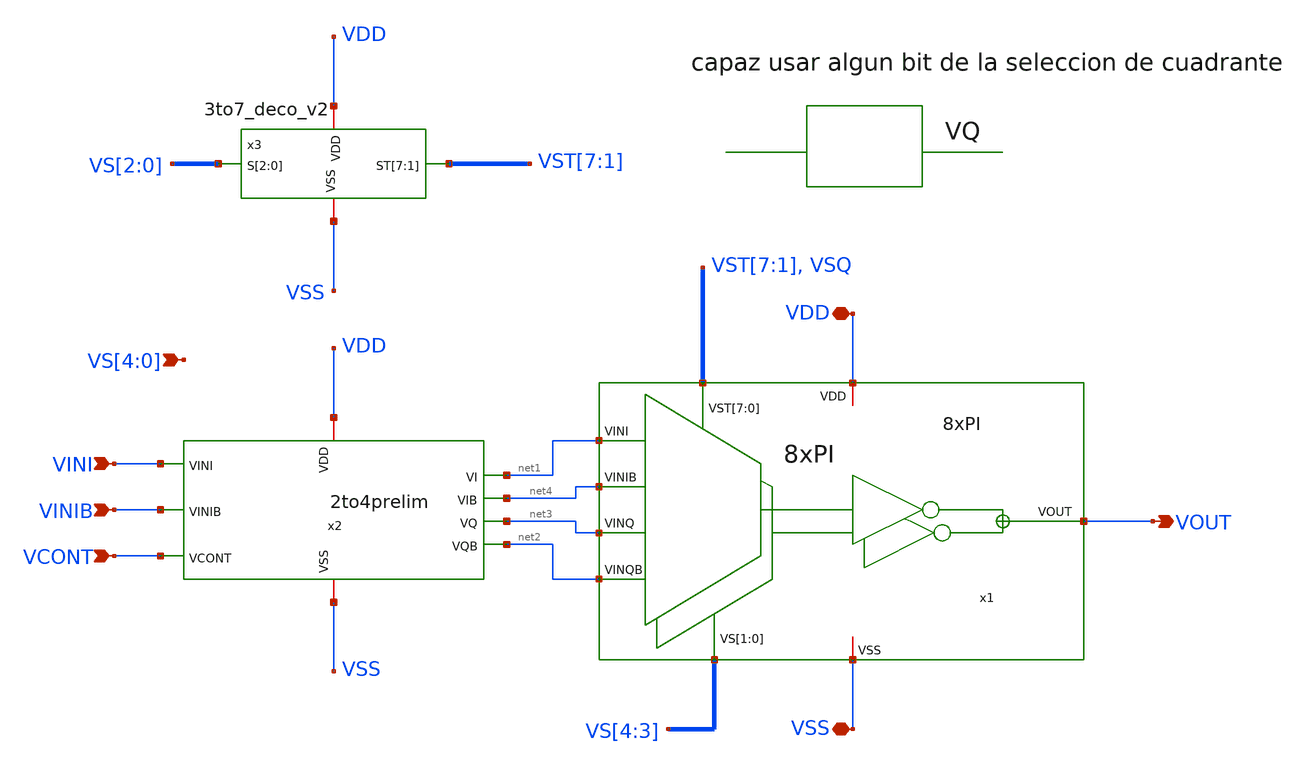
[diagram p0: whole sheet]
** sch_path: 8xPI_top/8xPI_top.sch
**.subckt 8xPI_top VINI VINIB VCONT VDD VSS VOUT VS[4],VS[3],VS[2],VS[1],VS[0]
*.ipin VINI
*.ipin VINIB
*.ipin VCONT
*.iopin VDD
*.iopin VSS
*.opin VOUT
*.ipin VS[4],VS[3],VS[2],VS[1],VS[0]
x1 net1 net4 net3 net2 VS[4] VS[3] VST[7] VST[6] VST[5] VST[4] VST[3] VST[2] VST[1] VSQ VOUT VDD VSS
+ 8xPI
x2 VDD net2 net3 VINI VSS VCONT net4 net1 VINIB 2to4prelim
x3 VST[7] VST[6] VST[5] VST[4] VST[3] VST[2] VST[1] VS[2] VS[1] VS[0] VDD VSS 3to7_deco_v2
**.ends
.end
